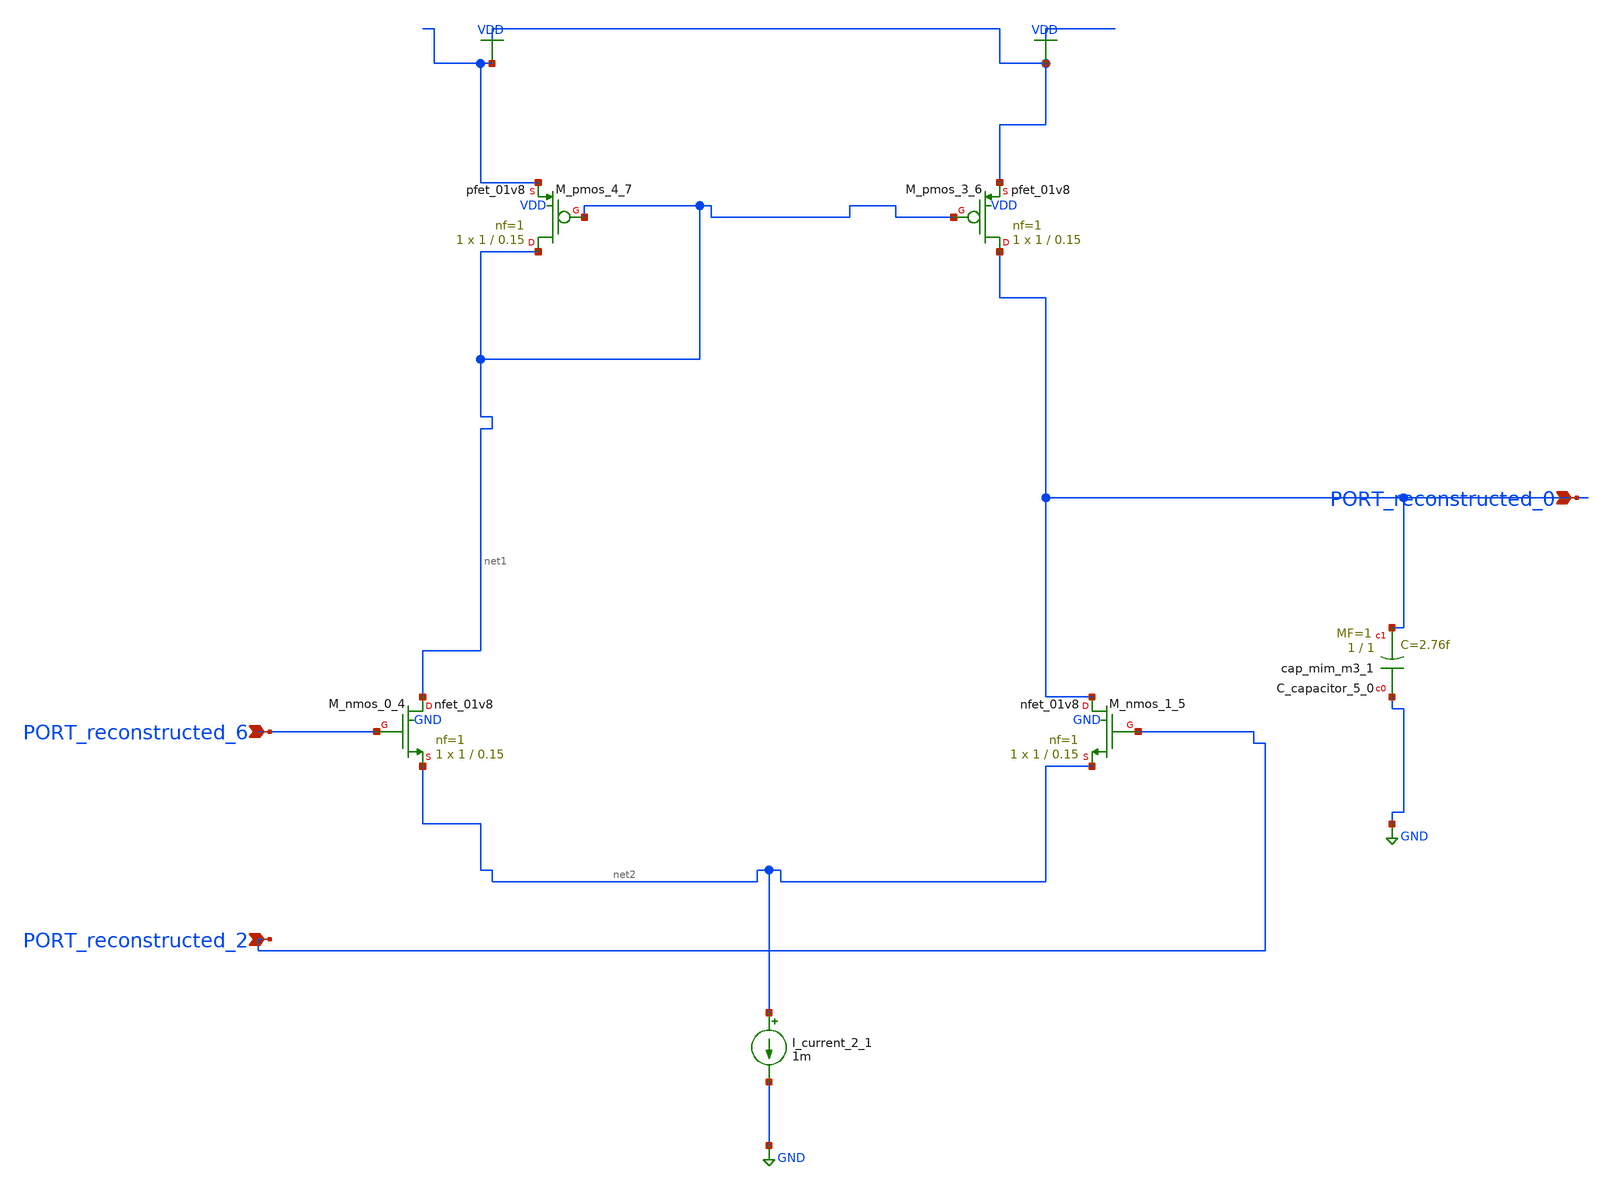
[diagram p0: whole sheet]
** sch_path: schematics/AMSNet/625.sch
**.subckt 625 PORT_reconstructed_2 PORT_reconstructed_0 PORT_reconstructed_6
*.ipin PORT_reconstructed_2
*.ipin PORT_reconstructed_0
*.ipin PORT_reconstructed_6
XC_capacitor_5_0 GND PORT_reconstructed_0 sky130_fd_pr__cap_mim_m3_1 W=1 L=1 MF=1 m=1
I_current_2_1 net2 GND 1m
XM_nmos_0_4 net1 PORT_reconstructed_6 net2 GND sky130_fd_pr__nfet_01v8 L=0.15 W=1 nf=1 ad='int((1 + 1)/2) * 1 / 1 * 0.29'
+ as='int((1 + 2)/2) * 1 / 1 * 0.29' pd='2*int((1 + 1)/2) * (1 / 1 + 0.29)' ps='2*int((1 + 2)/2) * (1 / 1 + 0.29)'
+ nrd='0.29 / 1 ' nrs='0.29 / 1 ' sa=0 sb=0 sd=0 mult=1 m=1
XM_nmos_1_5 PORT_reconstructed_0 PORT_reconstructed_2 net2 GND sky130_fd_pr__nfet_01v8 L=0.15 W=1 nf=1
+ ad='int((1 + 1)/2) * 1 / 1 * 0.29' as='int((1 + 2)/2) * 1 / 1 * 0.29' pd='2*int((1 + 1)/2) * (1 / 1 + 0.29)'
+ ps='2*int((1 + 2)/2) * (1 / 1 + 0.29)' nrd='0.29 / 1 ' nrs='0.29 / 1 ' sa=0 sb=0 sd=0 mult=1 m=1
XM_pmos_3_6 PORT_reconstructed_0 net1 VDD VDD sky130_fd_pr__pfet_01v8 L=0.15 W=1 nf=1 ad='int((1 + 1)/2) * 1 / 1 * 0.29'
+ as='int((1 + 2)/2) * 1 / 1 * 0.29' pd='2*int((1 + 1)/2) * (1 / 1 + 0.29)' ps='2*int((1 + 2)/2) * (1 / 1 + 0.29)'
+ nrd='0.29 / 1 ' nrs='0.29 / 1 ' sa=0 sb=0 sd=0 mult=1 m=1
XM_pmos_4_7 net1 net1 VDD VDD sky130_fd_pr__pfet_01v8 L=0.15 W=1 nf=1 ad='int((1 + 1)/2) * 1 / 1 * 0.29'
+ as='int((1 + 2)/2) * 1 / 1 * 0.29' pd='2*int((1 + 1)/2) * (1 / 1 + 0.29)' ps='2*int((1 + 2)/2) * (1 / 1 + 0.29)'
+ nrd='0.29 / 1 ' nrs='0.29 / 1 ' sa=0 sb=0 sd=0 mult=1 m=1
**.ends
.GLOBAL GND
.GLOBAL VDD
.end
